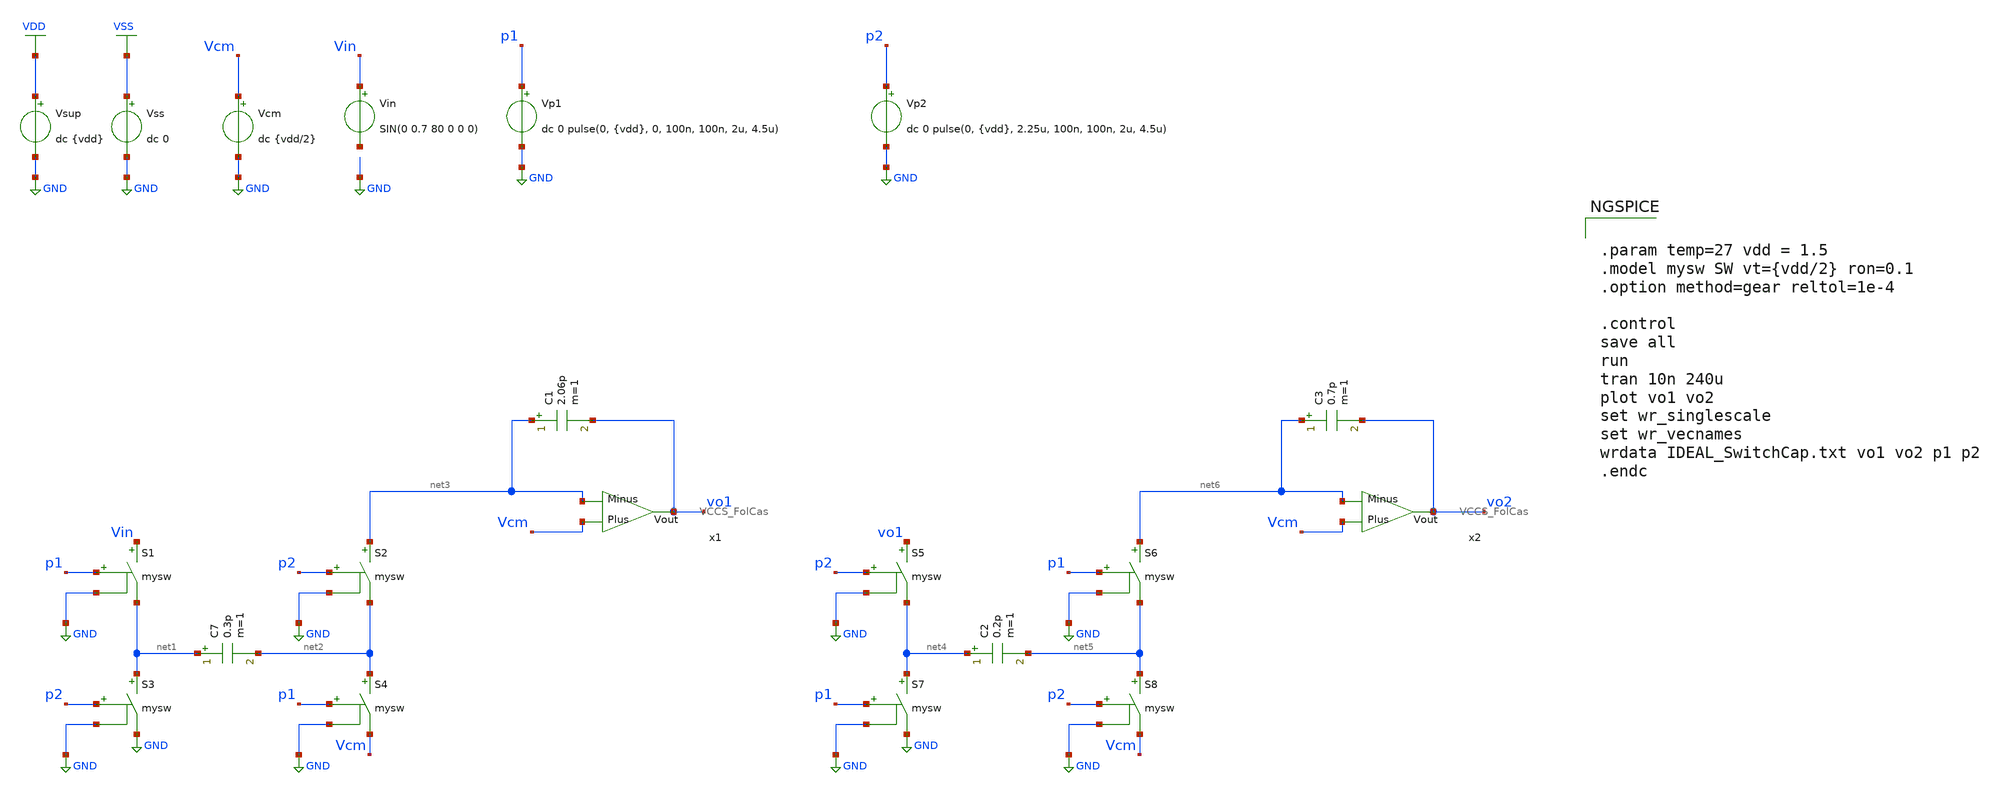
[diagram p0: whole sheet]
** sch_path: DSM/Schematics/Designs_Hrishi/RealCircuits/RealSwitchCap_using_FolCas_OTA.sch
* DSM/Schematics/IC_Designs_Hrishi/RealCircuits/Folded Cascode/FoldedCascodeOTA.sch:
* (c) 2024 Hrishikesh, @HSB
**.subckt RealSwitchCap_using_FolCas_OTA
Vcm Vcm GND dc {vdd/2}
Vin Vin net7 SIN(0 0.7 80 0 0 0)
S1 Vin net1 p1 GND mysw
S2 net3 net2 p2 GND mysw
S3 net1 GND p2 GND mysw
S4 net2 Vcm p1 GND mysw
C7 net1 net2 0.3p m=1
C1 net3 vo1 2.06p m=1
Vsup VDD GND dc {vdd}
Vss VSS GND dc 0
S5 vo1 net4 p2 GND mysw
S6 net6 net5 p1 GND mysw
S7 net4 GND p1 GND mysw
S8 net5 Vcm p2 GND mysw
C2 net4 net5 0.2p m=1
C3 net6 vo2 0.7p m=1
x1 Vcm vo1 net3 VCCS_FolCas
Vp1 p1 GND dc 0 pulse(0, {vdd}, 0, 100n, 100n, 2u, 4.5u)
Vp2 p2 GND dc 0 pulse(0, {vdd}, 2.25u, 100n, 100n, 2u, 4.5u)
x2 Vcm vo2 net6 VCCS_FolCas
**** begin user architecture code

.lib $::SG13G2_MODELS/cornerMOSlv.lib mos_tt
.lib $::SG13G2_MODELS/cornerRES.lib res_typ
.inc /foss/pdks/sg13g2/libs.ref/sg13g2_stdcell/spice/sg13g2_stdcell.spice



.param temp=27 vdd = 1.5
.model mysw SW vt={vdd/2} ron=0.1
.option method=gear reltol=1e-4

.control
save all
run
tran 10n 240u
plot vo1 vo2
set wr_singlescale
set wr_vecnames
wrdata IDEAL_SwitchCap.txt vo1 vo2 p1 p2
.endc


**** end user architecture code
**.ends

* expanding   symbol:
*+  /foss/designs/SecondOrder_SingleBit_DSM/DSM/IC_Designs_Hrishi/RealCircuits/VCCS_FolCas.sym # of pins=3
** sym_path: DSM/Schematics/Designs_Hrishi/RealCircuits/VCCS_FolCas.sym
** sch_path: DSM/Schematics/Designs_Hrishi/RealCircuits/VCCS_FolCas.sch
.subckt VCCS_FolCas Plus Vout Minus
*.ipin Minus
*.opin Vout
*.ipin Plus
Vdd v_dd GND 1.5
Vss v_ss GND 0
I0 v_dd net1 0.8u
x1 v_dd net1 Plus Minus Vout v_ss FoldedCascodeOTA
.ends


* expanding   symbol:  /foss/designs/CEMS_DSM/DSM/Schematics/IC_Designs_Hrishi/RealCircuits/Folded
*+ Cascode/FoldedCascodeOTA.sym # of pins=6
** sym_path: DSM/Schematics/IC_Designs_Hrishi/RealCircuits/Folded Cascode/FoldedCascodeOTA.sym
** sch_path: DSM/Schematics/IC_Designs_Hrishi/RealCircuits/Folded Cascode/FoldedCascodeOTA.sch
.subckt FoldedCascodeOTA VDD I PLUS MINUS Vout VSS
*.ipin PLUS
*.ipin MINUS
*.opin Vout
*.ipin VDD
*.ipin VSS
*.ipin I
XM1 net2 net4 VDD VDD sg13_lv_pmos w=0.272u l=0.5u ng=1 m=1 mm_ok=1
XM2 net1 PLUS net2 VDD sg13_lv_pmos w=0.136u l=0.5u ng=1 m=1 mm_ok=1
XM3 net6 MINUS net2 VDD sg13_lv_pmos w=0.136u l=0.5u ng=1 m=1 mm_ok=1
XM14 net6 net9 VSS VSS sg13_lv_nmos w=0.30u l=2u ng=1 m=1 mm_ok=1
XM13 Vout I net6 VSS sg13_lv_nmos w=0.15u l=2u ng=1 m=1 mm_ok=1
XM11 net7 I net1 VSS sg13_lv_nmos w=0.15u l=2u ng=1 m=1 mm_ok=1
XM12 net1 net9 VSS VSS sg13_lv_nmos w=0.30u l=2u ng=1 m=1 mm_ok=1
XM5 Vout net3 net5 VDD sg13_lv_pmos w=0.136u l=0.5u ng=1 m=1 mm_ok=1
XM4 net5 net4 VDD VDD sg13_lv_pmos w=0.136u l=0.5u ng=1 m=1 mm_ok=1
XM6 net4 net4 VDD VDD sg13_lv_pmos w=0.136u l=0.5u ng=1 m=1 mm_ok=1
XM8 net3 net3 net4 VDD sg13_lv_pmos w=0.136u l=0.5u ng=1 m=1 mm_ok=1
XM9 net8 net4 VDD VDD sg13_lv_pmos w=0.136u l=0.5u ng=1 m=1 mm_ok=1
XM10 net7 net3 net8 VDD sg13_lv_pmos w=0.136u l=0.5u ng=1 m=1 mm_ok=1
XM16 I I net9 VSS sg13_lv_nmos w=0.15u l=2u ng=1 m=1 mm_ok=1
XM15 net9 net9 VSS VSS sg13_lv_nmos w=0.15u l=2u ng=1 m=1 mm_ok=1
XM7 net3 net9 VSS VSS sg13_lv_nmos w=0.15u l=2u ng=1 m=1 mm_ok=1
XM18 VDD I net10 VSS sg13_lv_nmos w=0.15u l=2u ng=1 m=1 mm_ok=1
XM17 net10 net9 VSS VSS sg13_lv_nmos w=0.15u l=2u ng=1 m=1 mm_ok=1
.ends

.GLOBAL GND
.GLOBAL VDD
.GLOBAL VSS
.end
